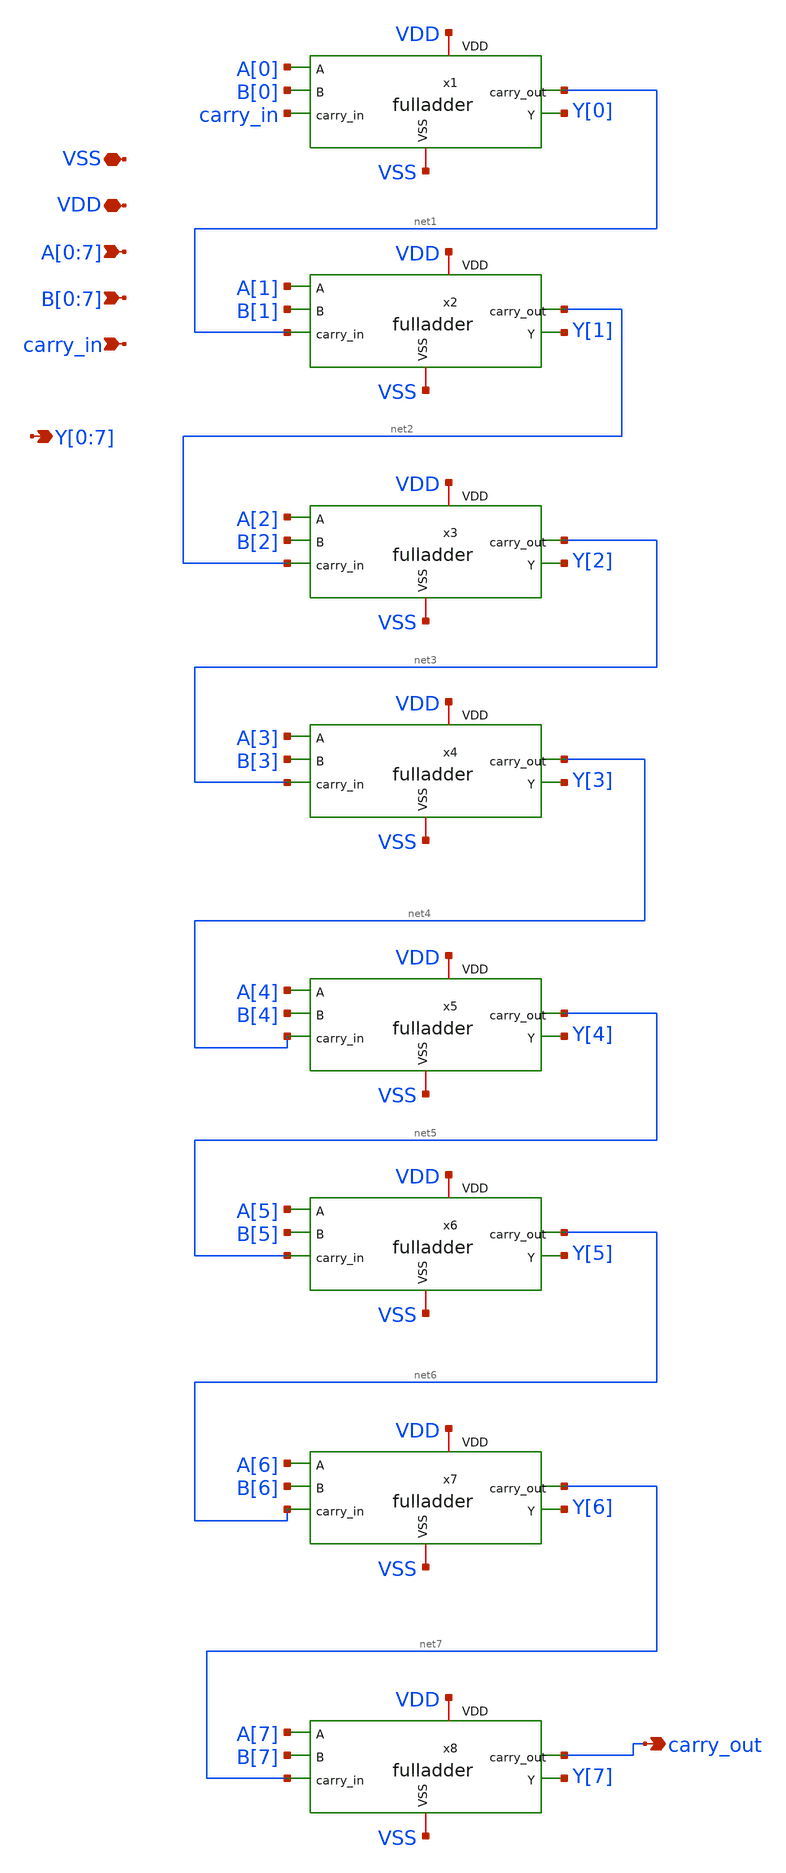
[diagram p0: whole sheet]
** sch_path: design/CONTROL_UNIT/xschem/carry_ripple_adder.sch
**.subckt carry_ripple_adder A[0],A[1],A[2],A[3],A[4],A[5],A[6],A[7]
*+ B[0],B[1],B[2],B[3],B[4],B[5],B[6],B[7] carry_in VDD VSS Y[0],Y[1],Y[2],Y[3],Y[4],Y[5],Y[6],Y[7] carry_out
*.ipin A[0],A[1],A[2],A[3],A[4],A[5],A[6],A[7]
*.ipin B[0],B[1],B[2],B[3],B[4],B[5],B[6],B[7]
*.ipin carry_in
*.iopin VDD
*.iopin VSS
*.opin Y[0],Y[1],Y[2],Y[3],Y[4],Y[5],Y[6],Y[7]
*.opin carry_out
x1 A[0] B[0] carry_in VDD VSS net1 Y[0] fulladder
x2 A[1] B[1] net1 VDD VSS net2 Y[1] fulladder
x3 A[2] B[2] net2 VDD VSS net3 Y[2] fulladder
x4 A[3] B[3] net3 VDD VSS net4 Y[3] fulladder
x5 A[4] B[4] net4 VDD VSS net5 Y[4] fulladder
x6 A[5] B[5] net5 VDD VSS net6 Y[5] fulladder
x7 A[6] B[6] net6 VDD VSS net7 Y[6] fulladder
x8 A[7] B[7] net7 VDD VSS carry_out Y[7] fulladder
**.ends
.end
